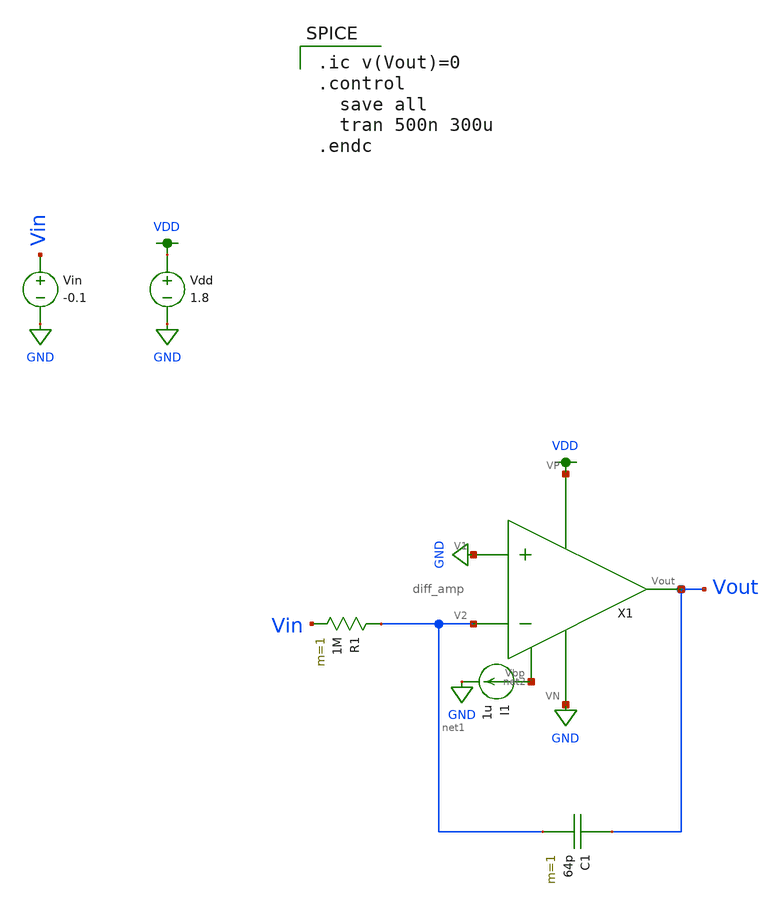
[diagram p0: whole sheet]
** sch_path: schematic/archive/integrator_test.sch
**.subckt integrator_test
Vdd VDD GND 1.8
Vin Vin GND -0.1
C1 Vout net1 64p m=1
X1 VDD net2 Vout GND net1 GND diff_amp
I1 net2 GND 1u
R1 net1 Vin 1M m=1
**** begin user architecture code

.ic v(Vout)=0
.control
  save all
  tran 500n 300u
.endc


.option wnflag=1
.param MC_SWITCH=0.0
.lib ~/skywater/skywater-pdk/libraries/sky130_fd_pr_ngspice/latest/models/sky130.lib.spice tt

**** end user architecture code
**.ends
.GLOBAL GND
.GLOBAL VDD
.end
